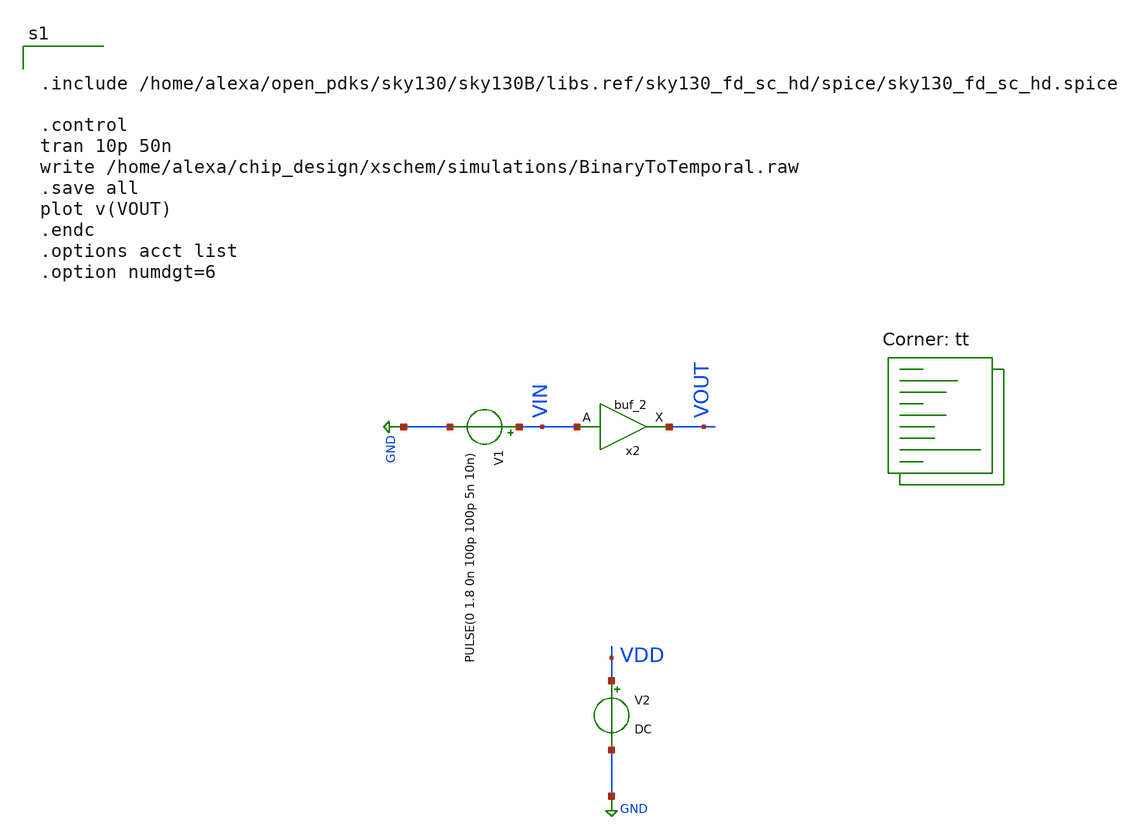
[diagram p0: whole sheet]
** sch_path: xschem/projects/BufferTest.sch
**.subckt BufferTest
V1 VIN GND PULSE(0 1.8 0n 100p 100p 5n 10n)
V2 VDD GND DC
x2 VIN 0 0 VDD VDD VOUT sky130_fd_sc_hd__buf_2
**** begin user architecture code


.include /home/alexa/open_pdks/sky130/sky130B/libs.ref/sky130_fd_sc_hd/spice/sky130_fd_sc_hd.spice

.control
tran 10p 50n
write /home/alexa/chip_design/xschem/simulations/BinaryToTemporal.raw
.save all
plot v(VOUT)
.endc
.options acct list
.option numdgt=6


.lib $::SKYWATER_MODELS/sky130.lib.spice tt
**** end user architecture code
**.ends
.GLOBAL GND
.end
